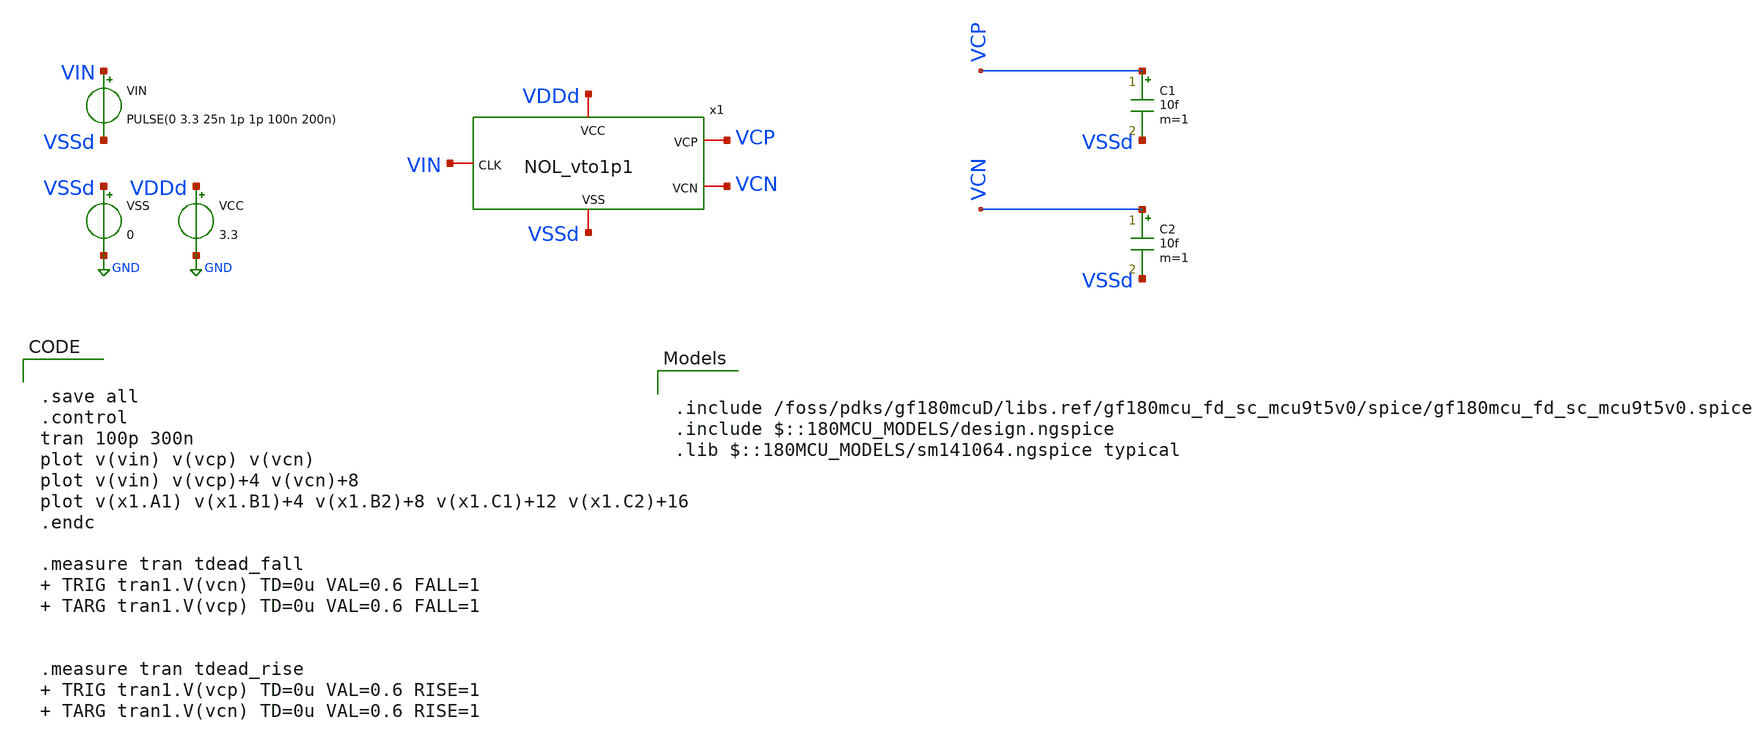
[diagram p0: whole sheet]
** sch_path: xschem/gf180_digital/NOL/tb_NOL_vto1p1.sch
**.subckt tb_NOL_vto1p1
VCC VDDd GND 3.3
VSS VSSd GND 0
VIN VIN VSSd PULSE(0 3.3 25n 1p 1p 100n 200n)
C1 VCP VSSd 10f m=1
C2 VCN VSSd 10f m=1
x1 VDDd VSSd VCP VIN VCN NOL_vto1p1
**** begin user architecture code


.save all
.control
tran 100p 300n
plot v(vin) v(vcp) v(vcn)
plot v(vin) v(vcp)+4 v(vcn)+8
plot v(x1.A1) v(x1.B1)+4 v(x1.B2)+8 v(x1.C1)+12 v(x1.C2)+16
.endc

.measure tran tdead_fall  TRIG tran1.V(vcn) TD=0u VAL=0.6 FALL=1  TARG tran1.V(vcp) TD=0u VAL=0.6
+ FALL=1


.measure tran tdead_rise  TRIG tran1.V(vcp) TD=0u VAL=0.6 RISE=1  TARG tran1.V(vcn) TD=0u VAL=0.6
+ RISE=1





.include /foss/pdks/gf180mcuD/libs.ref/gf180mcu_fd_sc_mcu9t5v0/spice/gf180mcu_fd_sc_mcu9t5v0.spice
.include $::180MCU_MODELS/design.ngspice
.lib $::180MCU_MODELS/sm141064.ngspice typical

**** end user architecture code
**.ends

* expanding   symbol:  gf180_digital/NOL/NOL_vto1p1.sym # of pins=5
** sym_path: xschem/gf180_digital/NOL/NOL_vto1p1.sym
** sch_path: xschem/gf180_digital/NOL/NOL_vto1p1.sch
.subckt NOL_vto1p1 VDDd VSSd VCP CLK VCN
*.iopin CLK
*.iopin VCP
*.iopin VCN
*.iopin VDDd
*.iopin VSSd
x11 B1 VSSd VDDd VSSd VDDd net1 gf180mcu_fd_sc_mcu9t5v0__inv_1
x12 net1 VSSd VDDd VSSd VDDd net3 gf180mcu_fd_sc_mcu9t5v0__inv_2
x13 net3 VSSd VDDd VSSd VDDd VCP gf180mcu_fd_sc_mcu9t5v0__inv_4
x14 A1 B1 VSSd VDDd VSSd VDDd C1 gf180mcu_fd_sc_mcu9t5v0__nor2_1
x15 VDDd VSSd C1 B2 large_delay_vto1p1
x4 VDDd VSSd C2 B1 large_delay_vto1p1
x1 B2 CLK VSSd VDDd VSSd VDDd C2 gf180mcu_fd_sc_mcu9t5v0__nor2_1
x3 CLK VSSd VDDd VSSd VDDd A1 gf180mcu_fd_sc_mcu9t5v0__inv_1
x5 B2 VSSd VDDd VSSd VDDd net2 gf180mcu_fd_sc_mcu9t5v0__inv_2
x6 net2 VSSd VDDd VSSd VDDd VCN gf180mcu_fd_sc_mcu9t5v0__inv_4
.ends


* expanding   symbol:  gf180_digital/large_delay/large_delay_vto1p1.sym # of pins=4
** sym_path: xschem/gf180_digital/large_delay/large_delay_vto1p1.sym
** sch_path: xschem/gf180_digital/large_delay/large_delay_vto1p1.sch
.subckt large_delay_vto1p1 VDDd VSSd VIN VOUT
*.iopin VIN
*.iopin VOUT
*.iopin VDDd
*.iopin VSSd
x1 VIN VOUT VDDd VDDd VSSd VSSd gf180mcu_fd_sc_mcu9t5v0__dlya_1
.ends

.GLOBAL GND
.end
